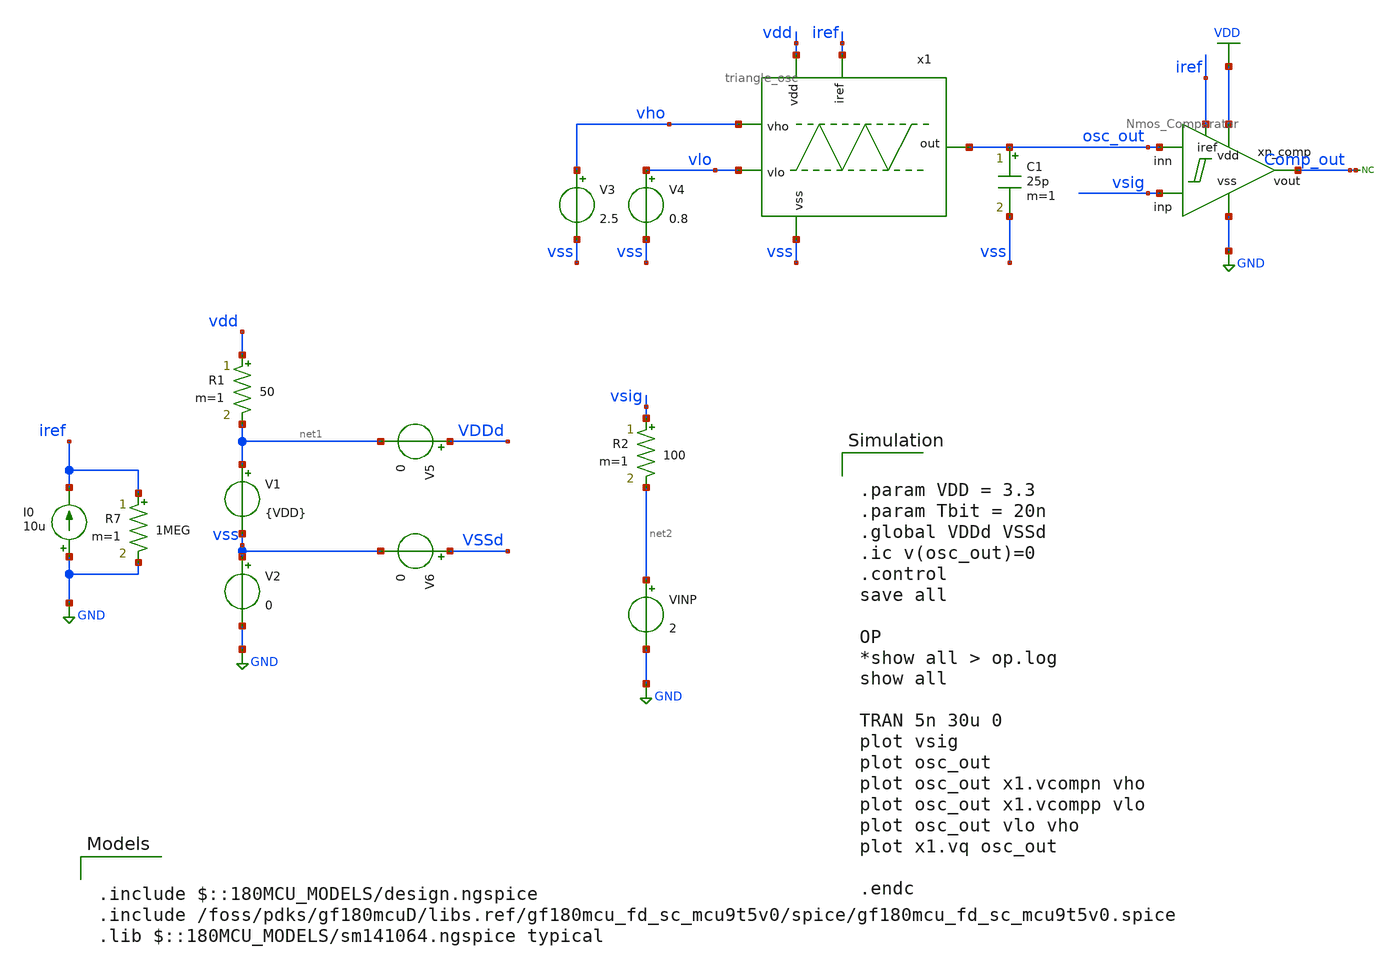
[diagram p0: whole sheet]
** sch_path: designs/libs/tb_analog/tb_top_sim/tb_osc_integration.sch
**.subckt tb_osc_integration
x1 vdd vho osc_out vlo iref vss triangle_osc
V1 net1 vss {VDD}
V2 vss GND 0
V3 vho vss 2.5
V4 vlo vss 0.8
I0 GND iref 10u
V5 VDDd net1 0
V6 VSSd vss 0
R1 vdd net1 50 m=1
xn_comp VDD Comp_out vsig GND osc_out iref Nmos_Comparator
* noconn Comp_out
VINP net2 GND 2
R2 vsig net2 100 m=1
R7 iref GND 1MEG m=1
C1 osc_out vss 25p m=1
**** begin user architecture code

.include $::180MCU_MODELS/design.ngspice
.include /foss/pdks/gf180mcuD/libs.ref/gf180mcu_fd_sc_mcu9t5v0/spice/gf180mcu_fd_sc_mcu9t5v0.spice
.lib $::180MCU_MODELS/sm141064.ngspice typical



.param VDD = 3.3
.param Tbit = 20n
.global VDDd VSSd
.ic v(osc_out)=0
.control
save all

OP
*show all > op.log
show all

TRAN 5n 30u 0
plot vsig
plot osc_out
plot osc_out x1.vcompn vho
plot osc_out x1.vcompp vlo
plot osc_out vlo vho
plot x1.vq osc_out

.endc


**** end user architecture code
**.ends

* expanding   symbol:  libs/core_analog/oscillator/triangle_osc.sym # of pins=6
** sym_path: libs/core_analog/oscillator/triangle_osc.sym
** sch_path: libs/core_analog/oscillator/triangle_osc.sch
.subckt triangle_osc vdd vho out vlo iref vss
*.ipin iref
*.ipin vss
*.ipin vho
*.ipin vlo
*.opin out
*.ipin vdd
XM1 net1 iref vss vss nfet_03v3 L=1u W=2.5u nf=1 ad='int((nf+1)/2) * W/nf * 0.18u' as='int((nf+2)/2) * W/nf * 0.18u'
+ pd='2*int((nf+1)/2) * (W/nf + 0.18u)' ps='2*int((nf+2)/2) * (W/nf + 0.18u)' nrd='0.18u / W' nrs='0.18u / W'
+ sa=0 sb=0 sd=0 m=3
XM8 net2 iref vss vss nfet_03v3 L=1u W=2.5u nf=1 ad='int((nf+1)/2) * W/nf * 0.18u' as='int((nf+2)/2) * W/nf * 0.18u'
+ pd='2*int((nf+1)/2) * (W/nf + 0.18u)' ps='2*int((nf+2)/2) * (W/nf + 0.18u)' nrd='0.18u / W' nrs='0.18u / W'
+ sa=0 sb=0 sd=0 m=3
XM4 net1 net1 vdd vdd pfet_03v3 L=1u W=4.5u nf=1 ad='int((nf+1)/2) * W/nf * 0.18u' as='int((nf+2)/2) * W/nf * 0.18u'
+ pd='2*int((nf+1)/2) * (W/nf + 0.18u)' ps='2*int((nf+2)/2) * (W/nf + 0.18u)' nrd='0.18u / W' nrs='0.18u / W'
+ sa=0 sb=0 sd=0 m=3
XM5 net3 net1 vdd vdd pfet_03v3 L=1u W=4.5u nf=1 ad='int((nf+1)/2) * W/nf * 0.18u' as='int((nf+2)/2) * W/nf * 0.18u'
+ pd='2*int((nf+1)/2) * (W/nf + 0.18u)' ps='2*int((nf+2)/2) * (W/nf + 0.18u)' nrd='0.18u / W' nrs='0.18u / W'
+ sa=0 sb=0 sd=0 m=3
XM6 out nq net3 vdd pfet_03v3 L=0.3u W=4u nf=1 ad='int((nf+1)/2) * W/nf * 0.18u' as='int((nf+2)/2) * W/nf * 0.18u'
+ pd='2*int((nf+1)/2) * (W/nf + 0.18u)' ps='2*int((nf+2)/2) * (W/nf + 0.18u)' nrd='0.18u / W' nrs='0.18u / W'
+ sa=0 sb=0 sd=0 m=2
XM7 out nq net2 vss nfet_03v3 L=0.3u W=4u nf=1 ad='int((nf+1)/2) * W/nf * 0.18u' as='int((nf+2)/2) * W/nf * 0.18u'
+ pd='2*int((nf+1)/2) * (W/nf + 0.18u)' ps='2*int((nf+2)/2) * (W/nf + 0.18u)' nrd='0.18u / W' nrs='0.18u / W'
+ sa=0 sb=0 sd=0 m=1
XM2 iref iref vss vss nfet_03v3 L=1u W=2.5u nf=1 ad='int((nf+1)/2) * W/nf * 0.18u' as='int((nf+2)/2) * W/nf * 0.18u'
+ pd='2*int((nf+1)/2) * (W/nf + 0.18u)' ps='2*int((nf+2)/2) * (W/nf + 0.18u)' nrd='0.18u / W' nrs='0.18u / W'
+ sa=0 sb=0 sd=0 m=1
XM10 net5 iref vss vss nfet_03v3 L=1u W=2.5u nf=1 ad='int((nf+1)/2) * W/nf * 0.18u' as='int((nf+2)/2) * W/nf * 0.18u'
+ pd='2*int((nf+1)/2) * (W/nf + 0.18u)' ps='2*int((nf+2)/2) * (W/nf + 0.18u)' nrd='0.18u / W' nrs='0.18u / W'
+ sa=0 sb=0 sd=0 m=1
XM9 net4 net1 vdd vdd pfet_03v3 L=1u W=4.5u nf=1 ad='int((nf+1)/2) * W/nf * 0.18u' as='int((nf+2)/2) * W/nf * 0.18u'
+ pd='2*int((nf+1)/2) * (W/nf + 0.18u)' ps='2*int((nf+2)/2) * (W/nf + 0.18u)' nrd='0.18u / W' nrs='0.18u / W'
+ sa=0 sb=0 sd=0 m=1
**** begin user architecture code

.include $::180MCU_MODELS/design.ngspice
.include /foss/pdks/gf180mcuD/libs.ref/gf180mcu_fd_sc_mcu9t5v0/spice/gf180mcu_fd_sc_mcu9t5v0.spice
.lib $::180MCU_MODELS/sm141064.ngspice typical

**** end user architecture code
xn_comp vdd vcompn vho vss out net4 Nmos_Comparator
xp_comp vdd vcompp out vss vlo net5 Pmos_Comparator
x1 vcompp q nq vcompn sr_latch
.ends


* expanding   symbol:  libs/core_analog/Comparator/Nmos_Comparator.sym # of pins=6
** sym_path: designs/libs/core_analog/Comparator/Nmos_Comparator.sym
** sch_path: designs/libs/core_analog/Comparator/Nmos_Comparator.sch
.subckt Nmos_Comparator vdd vout inp vss inn iref
*.ipin vss
*.ipin vdd
*.ipin iref
*.ipin inn
*.ipin inp
*.opin vout
XM3 net1 net1 vss vss nfet_03v3 L=1u W=3.5u nf=1 ad='int((nf+1)/2) * W/nf * 0.18u' as='int((nf+2)/2) * W/nf * 0.18u'
+ pd='2*int((nf+1)/2) * (W/nf + 0.18u)' ps='2*int((nf+2)/2) * (W/nf + 0.18u)' nrd='0.18u / W' nrs='0.18u / W'
+ sa=0 sb=0 sd=0 m=1
XM4 vout net1 vss vss nfet_03v3 L=1u W=3.5u nf=1 ad='int((nf+1)/2) * W/nf * 0.18u' as='int((nf+2)/2) * W/nf * 0.18u'
+ pd='2*int((nf+1)/2) * (W/nf + 0.18u)' ps='2*int((nf+2)/2) * (W/nf + 0.18u)' nrd='0.18u / W' nrs='0.18u / W'
+ sa=0 sb=0 sd=0 m=1
XM5 net2 inn net3 vss nfet_03v3 L=1u W=4u nf=1 ad='int((nf+1)/2) * W/nf * 0.18u' as='int((nf+2)/2) * W/nf * 0.18u'
+ pd='2*int((nf+1)/2) * (W/nf + 0.18u)' ps='2*int((nf+2)/2) * (W/nf + 0.18u)' nrd='0.18u / W' nrs='0.18u / W'
+ sa=0 sb=0 sd=0 m=1
XM6 net4 inp net3 vss nfet_03v3 L=1u W=4u nf=1 ad='int((nf+1)/2) * W/nf * 0.18u' as='int((nf+2)/2) * W/nf * 0.18u'
+ pd='2*int((nf+1)/2) * (W/nf + 0.18u)' ps='2*int((nf+2)/2) * (W/nf + 0.18u)' nrd='0.18u / W' nrs='0.18u / W'
+ sa=0 sb=0 sd=0 m=1
XM7 net1 net2 vdd vdd pfet_03v3 L=0.5u W=16.5u nf=4 ad='int((nf+1)/2) * W/nf * 0.18u' as='int((nf+2)/2) * W/nf * 0.18u'
+ pd='2*int((nf+1)/2) * (W/nf + 0.18u)' ps='2*int((nf+2)/2) * (W/nf + 0.18u)' nrd='0.18u / W' nrs='0.18u / W'
+ sa=0 sb=0 sd=0 m=1
XM9 net4 net4 vdd vdd pfet_03v3 L=0.5u W=10u nf=2 ad='int((nf+1)/2) * W/nf * 0.18u' as='int((nf+2)/2) * W/nf * 0.18u'
+ pd='2*int((nf+1)/2) * (W/nf + 0.18u)' ps='2*int((nf+2)/2) * (W/nf + 0.18u)' nrd='0.18u / W' nrs='0.18u / W'
+ sa=0 sb=0 sd=0 m=1
XM11 net2 net2 vdd vdd pfet_03v3 L=0.5u W=10u nf=2 ad='int((nf+1)/2) * W/nf * 0.18u' as='int((nf+2)/2) * W/nf * 0.18u'
+ pd='2*int((nf+1)/2) * (W/nf + 0.18u)' ps='2*int((nf+2)/2) * (W/nf + 0.18u)' nrd='0.18u / W' nrs='0.18u / W'
+ sa=0 sb=0 sd=0 m=1
XM12 vout net4 vdd vdd pfet_03v3 L=0.5u W=16.5u nf=4 ad='int((nf+1)/2) * W/nf * 0.18u' as='int((nf+2)/2) * W/nf * 0.18u'
+ pd='2*int((nf+1)/2) * (W/nf + 0.18u)' ps='2*int((nf+2)/2) * (W/nf + 0.18u)' nrd='0.18u / W' nrs='0.18u / W'
+ sa=0 sb=0 sd=0 m=1
XM1 net4 net2 vdd vdd pfet_03v3 L=0.5u W=10u nf=2 ad='int((nf+1)/2) * W/nf * 0.18u' as='int((nf+2)/2) * W/nf * 0.18u'
+ pd='2*int((nf+1)/2) * (W/nf + 0.18u)' ps='2*int((nf+2)/2) * (W/nf + 0.18u)' nrd='0.18u / W' nrs='0.18u / W'
+ sa=0 sb=0 sd=0 m=1
XM2 net2 net4 vdd vdd pfet_03v3 L=0.5u W=10u nf=2 ad='int((nf+1)/2) * W/nf * 0.18u' as='int((nf+2)/2) * W/nf * 0.18u'
+ pd='2*int((nf+1)/2) * (W/nf + 0.18u)' ps='2*int((nf+2)/2) * (W/nf + 0.18u)' nrd='0.18u / W' nrs='0.18u / W'
+ sa=0 sb=0 sd=0 m=1
XM8 iref iref vss vss nfet_03v3 L=1u W=2.5u nf=1 ad='int((nf+1)/2) * W/nf * 0.18u' as='int((nf+2)/2) * W/nf * 0.18u'
+ pd='2*int((nf+1)/2) * (W/nf + 0.18u)' ps='2*int((nf+2)/2) * (W/nf + 0.18u)' nrd='0.18u / W' nrs='0.18u / W'
+ sa=0 sb=0 sd=0 m=1
XM10 net3 iref vss vss nfet_03v3 L=1u W=5u nf=2 ad='int((nf+1)/2) * W/nf * 0.18u' as='int((nf+2)/2) * W/nf * 0.18u'
+ pd='2*int((nf+1)/2) * (W/nf + 0.18u)' ps='2*int((nf+2)/2) * (W/nf + 0.18u)' nrd='0.18u / W' nrs='0.18u / W'
+ sa=0 sb=0 sd=0 m=1
.ends


* expanding   symbol:  libs/core_analog/oscillator/sr_latch.sym # of pins=4
** sym_path: designs/libs/core_analog/oscillator/sr_latch.sym
** sch_path: designs/libs/core_analog/oscillator/sr_latch.sch
.subckt sr_latch R Q NOTQ S
*.ipin R
*.ipin S
*.opin Q
*.opin NOTQ
x1 R NOTQ VSSd VDDd VSSd VDDd Q gf180mcu_fd_sc_mcu9t5v0__nor2_2
x2 Q S VSSd VDDd VSSd VDDd NOTQ gf180mcu_fd_sc_mcu9t5v0__nor2_2
**** begin user architecture code

.include $::180MCU_MODELS/design.ngspice
.include /foss/pdks/gf180mcuD/libs.ref/gf180mcu_fd_sc_mcu9t5v0/spice/gf180mcu_fd_sc_mcu9t5v0.spice
.lib $::180MCU_MODELS/sm141064.ngspice typical

**** end user architecture code
.ends

.GLOBAL GND
.GLOBAL VDD
.end
